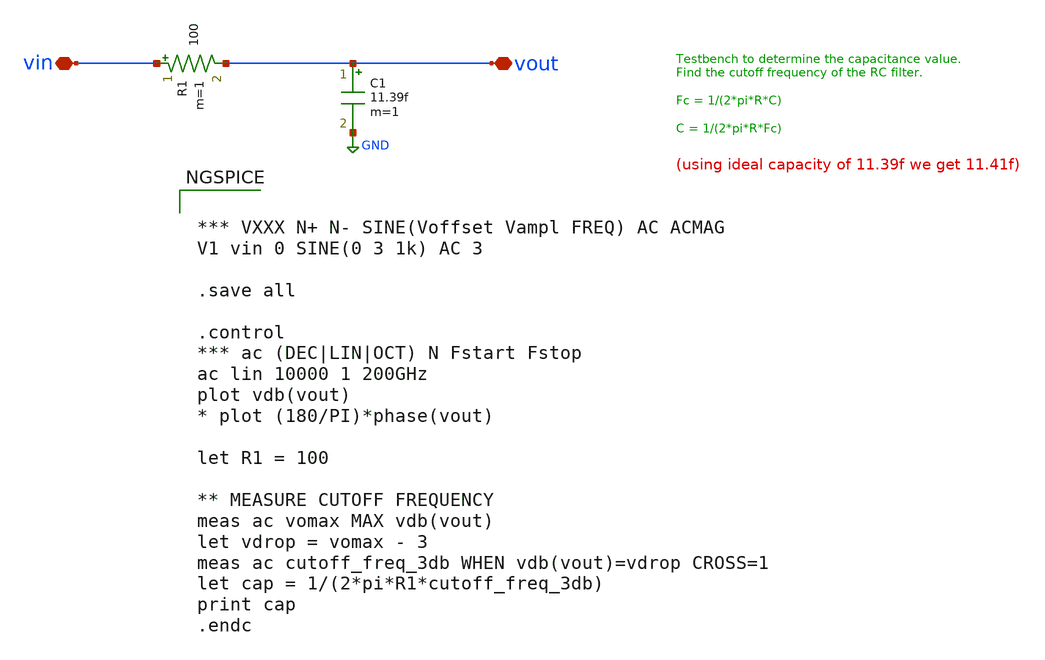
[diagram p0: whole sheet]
** sch_path: testdata/designs/sky130A/cap_vpp_04p4x04p6_l1m1m2_noshield/cap_vpp_04p4x04p6_l1m1m2_noshield__checkWithStdCap_tb.sch
**.subckt cap_vpp_04p4x04p6_l1m1m2_noshield__checkWithStdCap_tb vin vout
*.iopin vin
*.iopin vout
R1 vin vout 100 m=1
C1 vout GND 11.39f m=1
**** begin user architecture code


*** VXXX N+ N- SINE(Voffset Vampl FREQ) AC ACMAG
V1 vin 0 SINE(0 3 1k) AC 3

.save all

.control
*** ac (DEC|LIN|OCT) N Fstart Fstop
ac lin 10000 1 200GHz
plot vdb(vout)
* plot (180/PI)*phase(vout)

let R1 = 100

** MEASURE CUTOFF FREQUENCY
meas ac vomax MAX vdb(vout)
let vdrop = vomax - 3
meas ac cutoff_freq_3db WHEN vdb(vout)=vdrop CROSS=1
let cap = 1/(2*pi*R1*cutoff_freq_3db)
print cap
.endc



** opencircuitdesign pdks install
.lib $::SKYWATER_MODELS/sky130.lib.spice tt


**** end user architecture code
**.ends
.GLOBAL GND
.end
